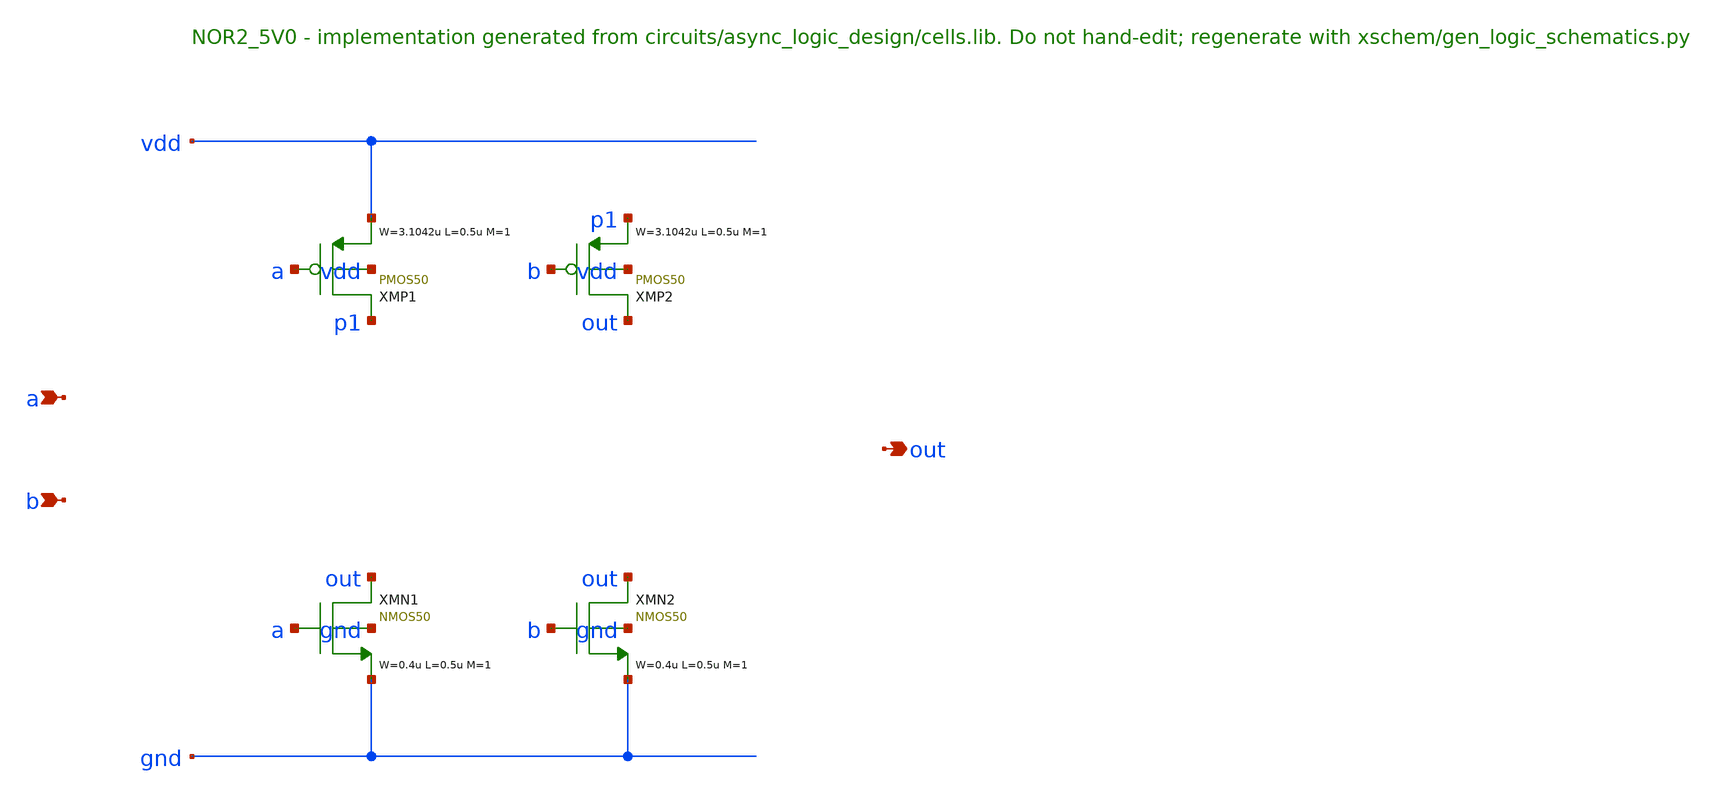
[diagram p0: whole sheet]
** sch_path: xschem/logic/NOR2_5V0.sch
**.subckt NOR2_5V0 a b out
*.ipin a
*.ipin b
*.opin out
XMP1 p1 a vdd vdd PMOS50 W=3.1042u L=0.5u M=1 MM_SIGMA=0
XMP2 out b p1 vdd PMOS50 W=3.1042u L=0.5u M=1 MM_SIGMA=0
XMN1 out a gnd gnd NMOS50 W=0.4u L=0.5u M=1 MM_SIGMA=0
XMN2 out b gnd gnd NMOS50 W=0.4u L=0.5u M=1 MM_SIGMA=0
**.ends
.end
